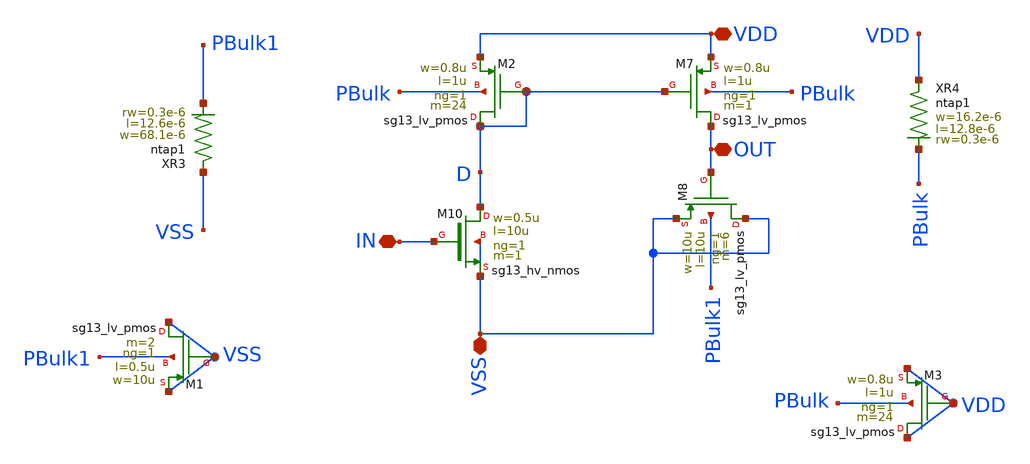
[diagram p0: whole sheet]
** sch_path: LVS/LVS_Sch/Delay.sch
**.subckt Delay VDD OUT VSS IN
*.iopin VDD
*.iopin OUT
*.iopin VSS
*.iopin IN
XM7 OUT D VDD PBulk sg13_lv_pmos w=0.8u l=1u ng=1 m=1 mm_ok=1
XM8 VSS OUT VSS PBulk1 sg13_lv_pmos w=10u l=10u ng=1 m=6 mm_ok=1
XM10 D IN VSS VSS sg13_hv_nmos w=0.5u l=10u ng=1 m=1 mm_ok=1
XM2 D D VDD PBulk sg13_lv_pmos w=0.8u l=1u ng=1 m=24 mm_ok=1
XR4 VDD PBulk ntap1 R=4.012 w=16.2e-6 l=12.8e-6 rw=0.3e-6
XR3 VSS PBulk1 ntap1 R=1.423 w=68.1e-6 l=12.6e-6 rw=0.3e-6
XM1 VSS VSS VSS PBulk1 sg13_lv_pmos w=10u l=0.5u ng=1 m=2 mm_ok=1
XM3 VDD VDD VDD PBulk sg13_lv_pmos w=0.8u l=1u ng=1 m=24 mm_ok=1
**.ends
.end
